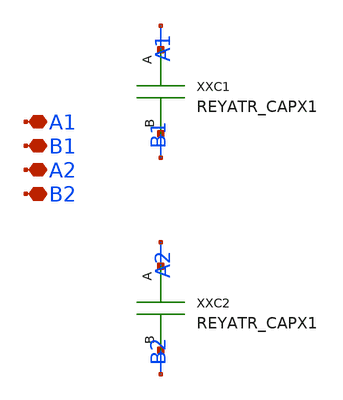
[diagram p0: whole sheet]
** sch_path: design/LELO_TEMP_SKY130A/REYATR_CAPTEST.sch
**.subckt REYATR_CAPTEST A1 B1 A2 B2
*.iopin A1
*.iopin B1
*.iopin A2
*.iopin B2
XXC1 A1 B1 REYATR_CAPX1
XXC2 A2 B2 REYATR_CAPX1
**.ends

* expanding   symbol:  LELO_TEMP_SKY130A/REYATR_CAPX1.sym # of pins=2
** sym_path: design/LELO_TEMP_SKY130A/REYATR_CAPX1.sym
** sch_path: design/LELO_TEMP_SKY130A/REYATR_CAPX1.sch
.subckt REYATR_CAPX1 A B
*.iopin A
*.iopin B
XC1 B A sky130_fd_pr__cap_mim_m3_1 W=4.8 L=5 MF=1 m=1
.ends

.end
